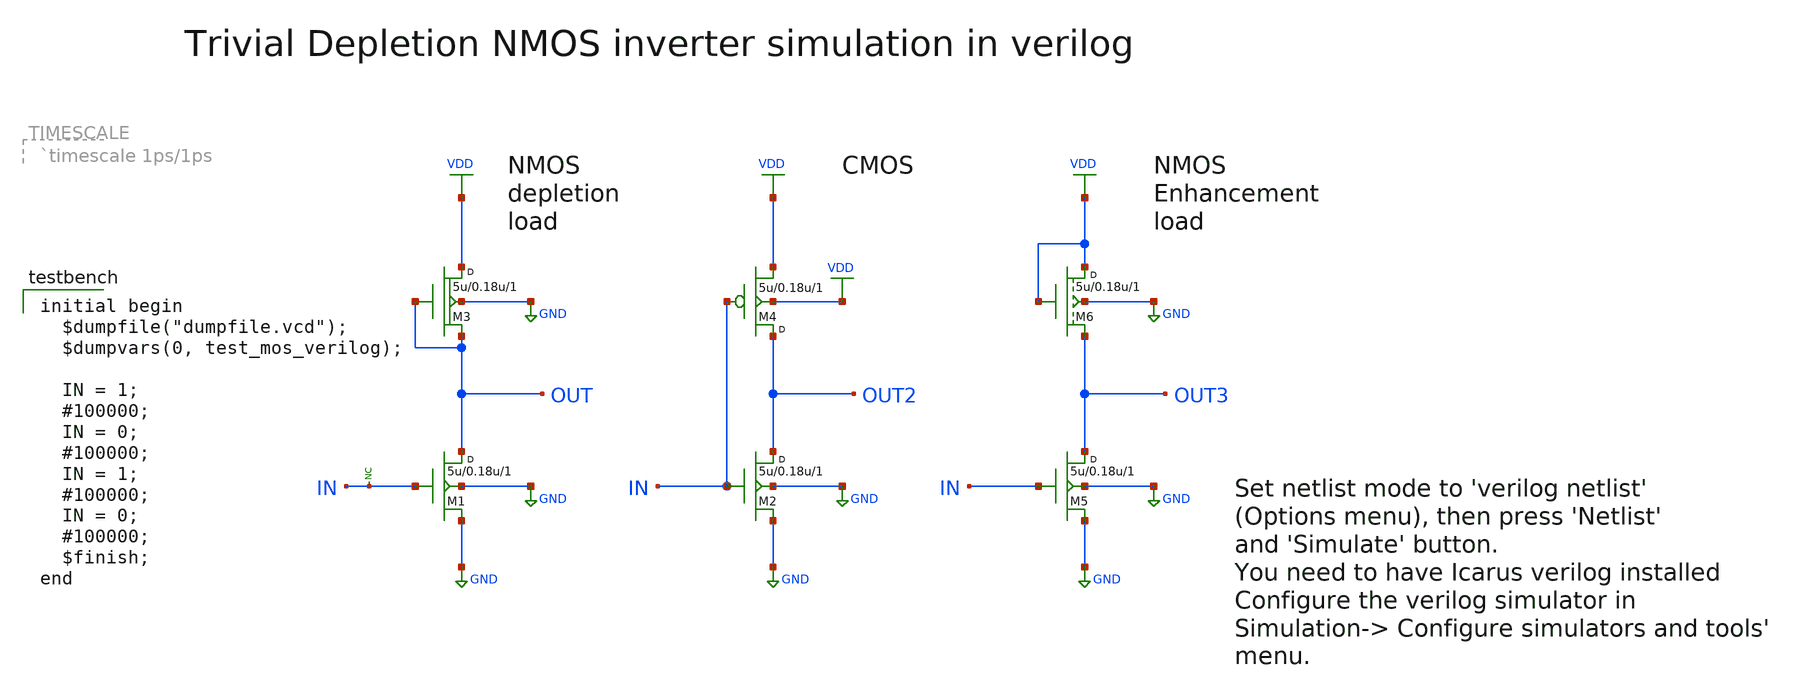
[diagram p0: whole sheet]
** sch_path: xschem_library_oa/logic/test_mos_verilog/schematic/test_mos_verilog.sch
* Copyright (C) 1998-2024 Stefan Frederik Schippers
* This program is free software; you can redistribute it and/or modify
* it under the terms of the GNU General Public License as published by
* the Free Software Foundation; either version 2 of the License, or
* (at your option) any later version.
* This program is distributed in the hope that it will be useful,
* but WITHOUT ANY WARRANTY; without even the implied warranty of
* MERCHANTABILITY or FITNESS FOR A PARTICULAR PURPOSE.  See the
* GNU General Public License for more details.
* You should have received a copy of the GNU General Public License
* along with this program; if not, write to the Free Software
**.subckt test_mos_verilog
M1 OUT IN GND GND nmos w=5u l=0.18u m=1
M3 VDD OUT OUT GND nmos w=5u l=0.18u m=1
M2 OUT2 IN GND GND nmos w=5u l=0.18u m=1
M4 OUT2 IN VDD VDD pmos w=5u l=0.18u m=1
* noconn IN
M5 OUT3 IN GND GND nmos w=5u l=0.18u m=1
M6 VDD VDD OUT3 GND nmos w=5u l=0.18u m=1
**** begin user architecture code

initial begin
  $dumpfile("dumpfile.vcd");
  $dumpvars(0, test_mos_verilog);

  IN = 1;
  #100000;
  IN = 0;
  #100000;
  IN = 1;
  #100000;
  IN = 0;
  #100000;
  $finish;
end


**** end user architecture code
**.ends
.GLOBAL GND
.GLOBAL VDD
.end
